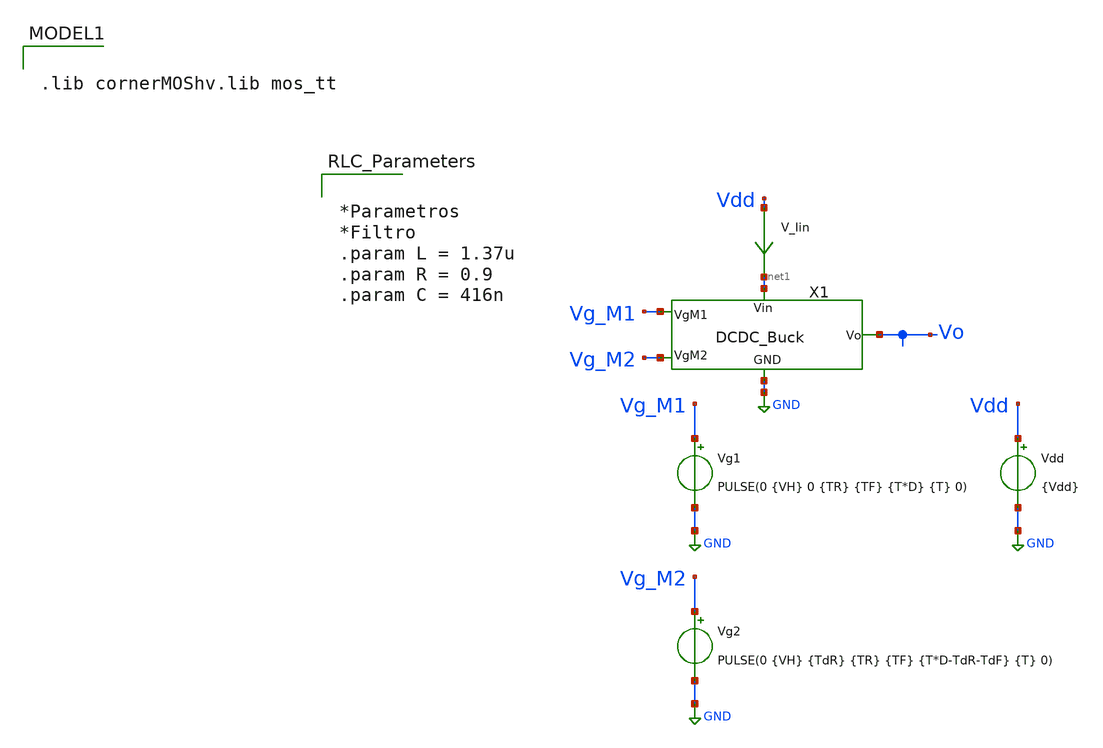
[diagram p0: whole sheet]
** sch_path: xschem/TB_DCDCBuck.sch
**.subckt TB_DCDCBuck
X1 Vg_M1 Vg_M2 GND net1 Vo DCDC_Buck
Vdd Vdd GND {Vdd}
Vg2 Vg_M2 GND PULSE(0 {VH} {TdR} {TR} {TF} {T*D-TdR-TdF} {T} 0)
Vg1 Vg_M1 GND PULSE(0 {VH} 0 {TR} {TF} {T*D} {T} 0)
V_Iin Vdd net1 0
.save i(v_iin)
**** begin user architecture code


.param temp=27
.param mult_M1 = 2400
.param w_M1 =10u
*.param l_M1 = 0.2u ** Posee mayor capacidad de corriente, pero en sub-umbral conduce mucha
*+ corriente
.param l_M1 = 0.22u
.param ng_M1 = 1

.param mult_M2 = 1200
.param w_M2 =10u
.param l_M2 =0.25u
.param ng_M2 =1







.param Vdd = 3.3
.param VH = 3.3
.param Del = 0

.param D = 0.42
.param T = 1u
.param TR = 7n
.param TF = 7n
.param TdR = 5n
.param TdF = 5n


.param temp = 27





.save all  @n.x1.xm1.nsg13_hv_pmos[ids]  @n.x1.xm2.nsg13_hv_nmos[ids]
.param SimTime = 5u

.control
reset
set color0 = white
tran 1n 20u
let Io = i(v.x1.V_Io)
let Id_M1 = @n.x1.xm1.nsg13_hv_pmos[ids]
let Id_M2 = @n.x1.xm2.nsg13_hv_nmos[ids]
let Po = Io*v(Vo)
let I_in = i(V_Iin)
let Pin = I_in*v(Vdd)
let Vsd_M1 = v(Vdd) - v(x1.Vc)
let Vds_M2 = v(x1.Vc)
let P_M1 = Vsd_M1*Id_M1
let P_M2 = -Vds_M2*Id_M2
let DataMeasBegin = SimTime-1u

meas tran Vo_mean AVG v(Vo) from=10u to=20u
meas tran Io_mean AVG Io from=10u to=20u
meas tran Po_mean AVG Po from=10u to=20u
meas tran Pin_mean AVG Pin from=10u to=20u
meas tran P_M1_mean AVG P_M1 from=10u to=20u
meas tran P_M2_mean AVG P_M2 from=10u to=20u

let eff = 100*Po_mean/Pin_mean
let loss_M1 = 100*P_M1_mean/Pin_mean
let loss_M2 = 100*P_M2_mean/Pin_mean
let sumaPot = eff+loss_M1+loss_M2
print eff loss_M1 loss_M2 sumaPot

plot Io i(v.x1.V_IL)
plot Id_M1 Id_M2
plot v(Vo)
plot Po Pin
*plot P_M1 P_M2
plot v(x1.Vc)
plot v(Vg_M1) v(Vg_M2)
.endc



.end



.lib cornerMOShv.lib mos_tt



*Parametros
*Filtro
.param L = 1.37u
.param R = 0.9
.param C = 416n




**** end user architecture code
**.ends

* expanding   symbol:
*+  /workspaces/usm-vlsi-tools/shared_xserver/simulations/IHP-sg13g2/Simulaciones/Modulos/DCDC_Buck.sym # of pins=5
** sym_path: /workspaces/usm-vlsi-tools/shared_xserver/simulations/IHP-sg13g2/Simulaciones/Modulos/DCDC_Buck.sym
** sch_path: /workspaces/usm-vlsi-tools/shared_xserver/simulations/IHP-sg13g2/Simulaciones/Modulos/DCDC_Buck.sch
.subckt DCDC_Buck VgM1 VgM2 GND Vin Vo
*.iopin Vin
*.ipin VgM1
*.ipin VgM2
*.iopin Vo
*.iopin GND
XM2 GND VgM2 Vc GND sg13_hv_nmos w={w_M2} l={l_M2} ng={ng_M2} m={mult_M2} mm_ok=1
XM1 Vc VgM1 Vin Vin sg13_hv_pmos w={w_M1} l={l_M1} ng={ng_M1} m={mult_M1} mm_ok=1
L1 net2 net1 {L} m=1
C1 net1 GND {C} m=1
V_Io net1 Vo 0
.save i(v_io)
V_IL Vc net2 0
.save i(v_il)
R1 Vo GND {R} m=1
.ends

.GLOBAL GND
.end
